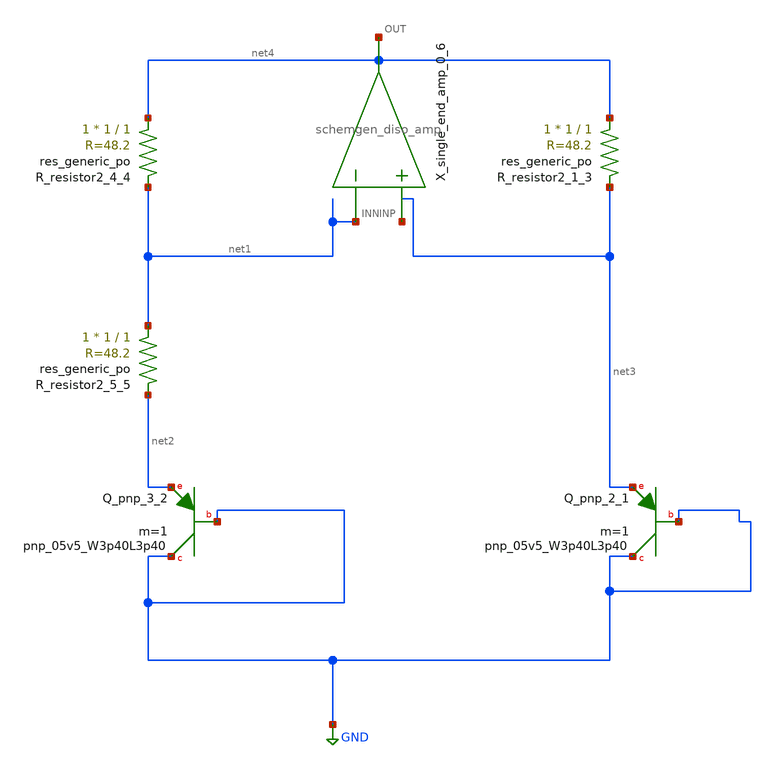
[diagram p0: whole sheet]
** sch_path: schematics/Image2Net/068.sch
**.subckt 068
XQ_pnp_2_1 GND GND net3 sky130_fd_pr__pnp_05v5_W3p40L3p40 m=1
XQ_pnp_3_2 GND GND net2 sky130_fd_pr__pnp_05v5_W3p40L3p40 m=1
XR_resistor2_1_3 net4 net3 sky130_fd_pr__res_generic_po W=1 L=1 m=1
XR_resistor2_4_4 net4 net1 sky130_fd_pr__res_generic_po W=1 L=1 m=1
XR_resistor2_5_5 net1 net2 sky130_fd_pr__res_generic_po W=1 L=1 m=1
X_single_end_amp_0_6 net3 net1 net4 schemgen_diso_amp
**.ends

* expanding   symbol:  schemgen_diso_amp.sym # of pins=3
** sym_path: symbols/schemgen_diso_amp.sym
.subckt schemgen_diso_amp INP INN OUT
* SchemGen ideal op-amp: Vout = 1e5 * (V(INP) - V(INN))
E1 OUT 0 INP INN 1e5
.ends schemgen_diso_amp
.GLOBAL GND
.end
